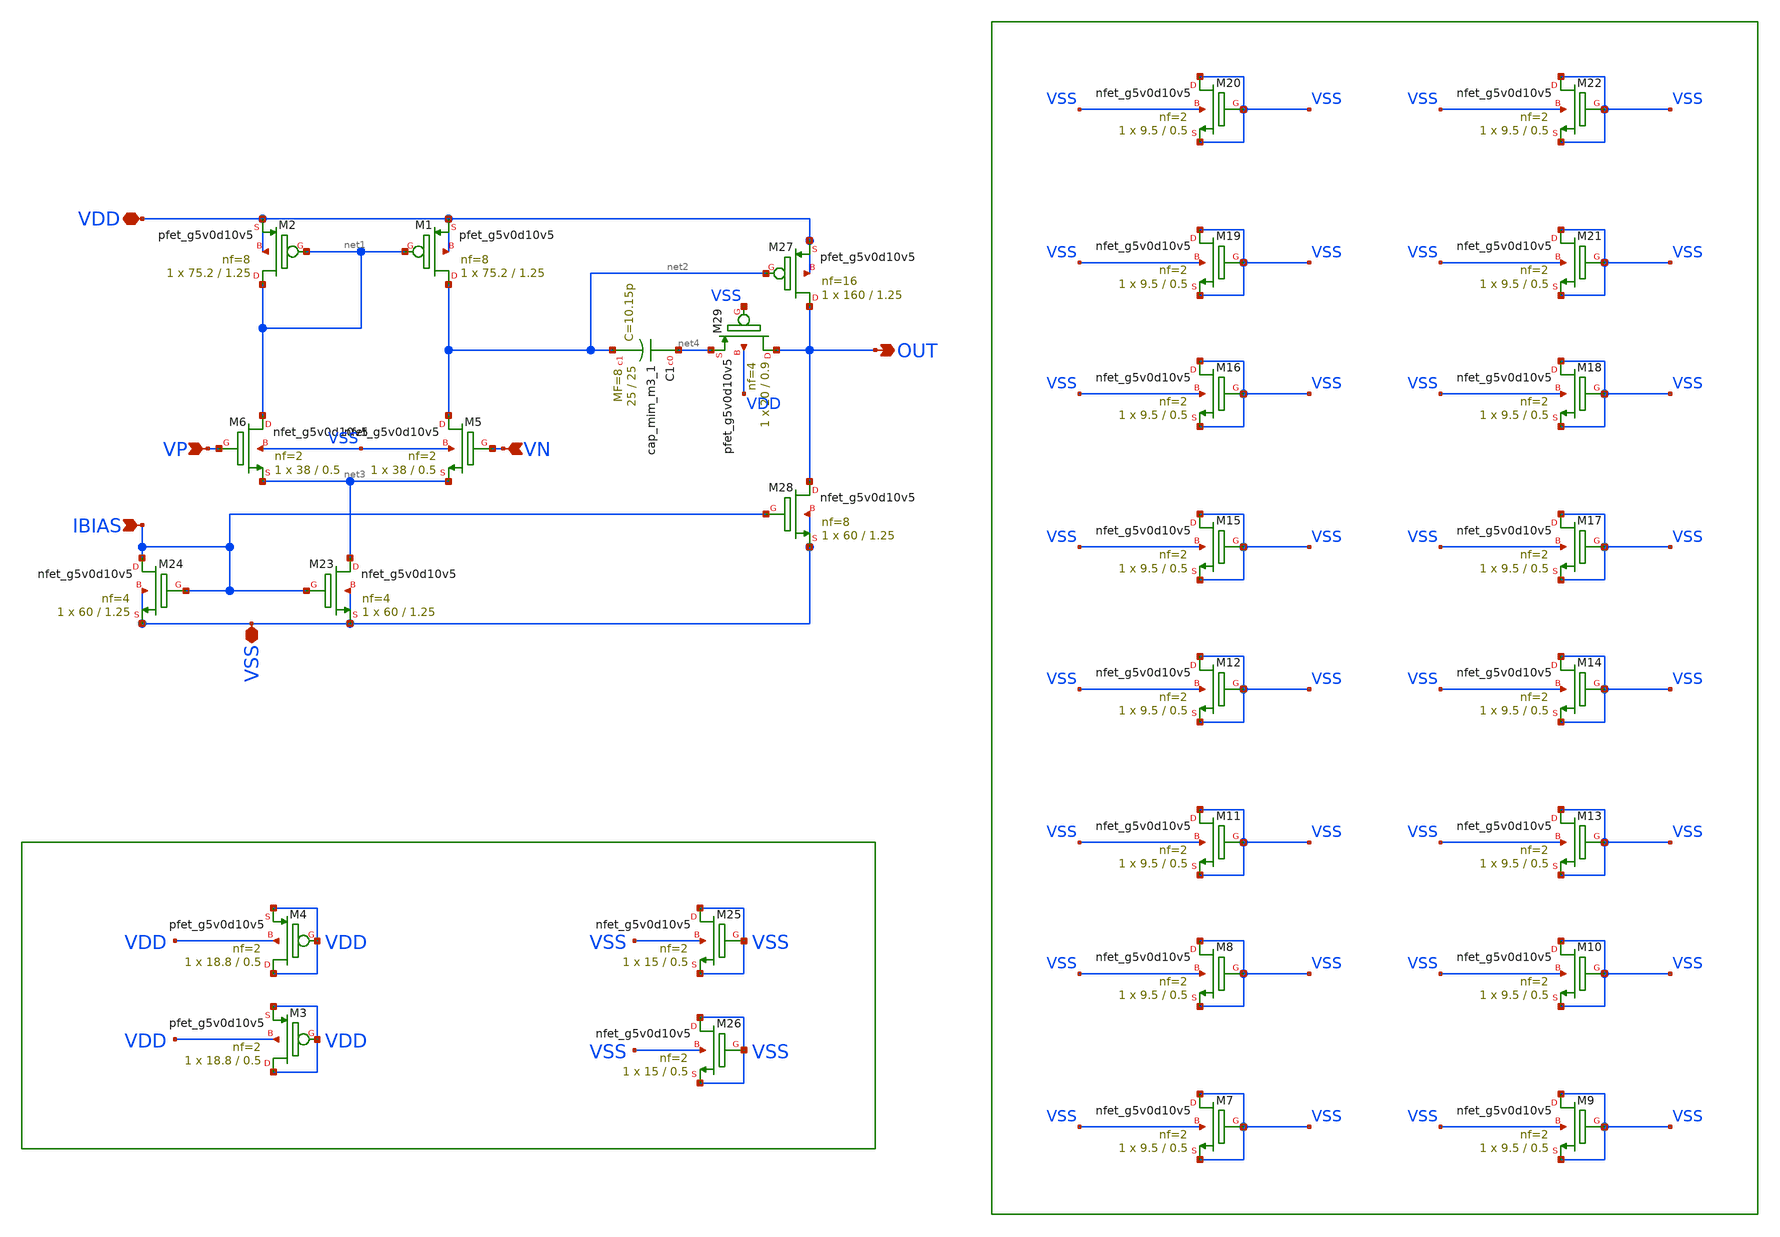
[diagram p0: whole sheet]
** sch_path: xschem/error-amplifier2/schematics/1st-stage.sch
**.subckt 1st-stage VDD VP VN IBIAS VSS OUT
*.iopin VDD
*.ipin VP
*.ipin VN
*.ipin IBIAS
*.iopin VSS
*.opin OUT
XM1 net2 net1 VDD VDD sky130_fd_pr__pfet_g5v0d10v5 L=1.25 W=75.2 nf=8 ad='int((nf+1)/2) * W/nf * 0.29'
+ as='int((nf+2)/2) * W/nf * 0.29' pd='2*int((nf+1)/2) * (W/nf + 0.29)' ps='2*int((nf+2)/2) * (W/nf + 0.29)'
+ nrd='0.29 / W' nrs='0.29 / W' sa=0 sb=0 sd=0 mult=1 m=1
XM2 net1 net1 VDD VDD sky130_fd_pr__pfet_g5v0d10v5 L=1.25 W=75.2 nf=8 ad='int((nf+1)/2) * W/nf * 0.29'
+ as='int((nf+2)/2) * W/nf * 0.29' pd='2*int((nf+1)/2) * (W/nf + 0.29)' ps='2*int((nf+2)/2) * (W/nf + 0.29)'
+ nrd='0.29 / W' nrs='0.29 / W' sa=0 sb=0 sd=0 mult=1 m=1
XM3 VDD VDD VDD VDD sky130_fd_pr__pfet_g5v0d10v5 L=0.5 W=18.8 nf=2 ad='int((nf+1)/2) * W/nf * 0.29' as='int((nf+2)/2) * W/nf * 0.29'
+ pd='2*int((nf+1)/2) * (W/nf + 0.29)' ps='2*int((nf+2)/2) * (W/nf + 0.29)' nrd='0.29 / W' nrs='0.29 / W'
+ sa=0 sb=0 sd=0 mult=1 m=1
XM4 VDD VDD VDD VDD sky130_fd_pr__pfet_g5v0d10v5 L=0.5 W=18.8 nf=2 ad='int((nf+1)/2) * W/nf * 0.29' as='int((nf+2)/2) * W/nf * 0.29'
+ pd='2*int((nf+1)/2) * (W/nf + 0.29)' ps='2*int((nf+2)/2) * (W/nf + 0.29)' nrd='0.29 / W' nrs='0.29 / W'
+ sa=0 sb=0 sd=0 mult=1 m=1
XM5 net2 VN net3 VSS sky130_fd_pr__nfet_g5v0d10v5 L=0.5 W=38 nf=2 ad='int((nf+1)/2) * W/nf * 0.29' as='int((nf+2)/2) * W/nf * 0.29'
+ pd='2*int((nf+1)/2) * (W/nf + 0.29)' ps='2*int((nf+2)/2) * (W/nf + 0.29)' nrd='0.29 / W' nrs='0.29 / W'
+ sa=0 sb=0 sd=0 mult=1 m=1
XM6 net1 VP net3 VSS sky130_fd_pr__nfet_g5v0d10v5 L=0.5 W=38 nf=2 ad='int((nf+1)/2) * W/nf * 0.29' as='int((nf+2)/2) * W/nf * 0.29'
+ pd='2*int((nf+1)/2) * (W/nf + 0.29)' ps='2*int((nf+2)/2) * (W/nf + 0.29)' nrd='0.29 / W' nrs='0.29 / W'
+ sa=0 sb=0 sd=0 mult=1 m=1
XM7 VSS VSS VSS VSS sky130_fd_pr__nfet_g5v0d10v5 L=0.5 W=9.5 nf=2 ad='int((nf+1)/2) * W/nf * 0.29' as='int((nf+2)/2) * W/nf * 0.29'
+ pd='2*int((nf+1)/2) * (W/nf + 0.29)' ps='2*int((nf+2)/2) * (W/nf + 0.29)' nrd='0.29 / W' nrs='0.29 / W'
+ sa=0 sb=0 sd=0 mult=1 m=1
XM8 VSS VSS VSS VSS sky130_fd_pr__nfet_g5v0d10v5 L=0.5 W=9.5 nf=2 ad='int((nf+1)/2) * W/nf * 0.29' as='int((nf+2)/2) * W/nf * 0.29'
+ pd='2*int((nf+1)/2) * (W/nf + 0.29)' ps='2*int((nf+2)/2) * (W/nf + 0.29)' nrd='0.29 / W' nrs='0.29 / W'
+ sa=0 sb=0 sd=0 mult=1 m=1
XM9 VSS VSS VSS VSS sky130_fd_pr__nfet_g5v0d10v5 L=0.5 W=9.5 nf=2 ad='int((nf+1)/2) * W/nf * 0.29' as='int((nf+2)/2) * W/nf * 0.29'
+ pd='2*int((nf+1)/2) * (W/nf + 0.29)' ps='2*int((nf+2)/2) * (W/nf + 0.29)' nrd='0.29 / W' nrs='0.29 / W'
+ sa=0 sb=0 sd=0 mult=1 m=1
XM10 VSS VSS VSS VSS sky130_fd_pr__nfet_g5v0d10v5 L=0.5 W=9.5 nf=2 ad='int((nf+1)/2) * W/nf * 0.29' as='int((nf+2)/2) * W/nf * 0.29'
+ pd='2*int((nf+1)/2) * (W/nf + 0.29)' ps='2*int((nf+2)/2) * (W/nf + 0.29)' nrd='0.29 / W' nrs='0.29 / W'
+ sa=0 sb=0 sd=0 mult=1 m=1
XM11 VSS VSS VSS VSS sky130_fd_pr__nfet_g5v0d10v5 L=0.5 W=9.5 nf=2 ad='int((nf+1)/2) * W/nf * 0.29' as='int((nf+2)/2) * W/nf * 0.29'
+ pd='2*int((nf+1)/2) * (W/nf + 0.29)' ps='2*int((nf+2)/2) * (W/nf + 0.29)' nrd='0.29 / W' nrs='0.29 / W'
+ sa=0 sb=0 sd=0 mult=1 m=1
XM12 VSS VSS VSS VSS sky130_fd_pr__nfet_g5v0d10v5 L=0.5 W=9.5 nf=2 ad='int((nf+1)/2) * W/nf * 0.29' as='int((nf+2)/2) * W/nf * 0.29'
+ pd='2*int((nf+1)/2) * (W/nf + 0.29)' ps='2*int((nf+2)/2) * (W/nf + 0.29)' nrd='0.29 / W' nrs='0.29 / W'
+ sa=0 sb=0 sd=0 mult=1 m=1
XM13 VSS VSS VSS VSS sky130_fd_pr__nfet_g5v0d10v5 L=0.5 W=9.5 nf=2 ad='int((nf+1)/2) * W/nf * 0.29' as='int((nf+2)/2) * W/nf * 0.29'
+ pd='2*int((nf+1)/2) * (W/nf + 0.29)' ps='2*int((nf+2)/2) * (W/nf + 0.29)' nrd='0.29 / W' nrs='0.29 / W'
+ sa=0 sb=0 sd=0 mult=1 m=1
XM14 VSS VSS VSS VSS sky130_fd_pr__nfet_g5v0d10v5 L=0.5 W=9.5 nf=2 ad='int((nf+1)/2) * W/nf * 0.29' as='int((nf+2)/2) * W/nf * 0.29'
+ pd='2*int((nf+1)/2) * (W/nf + 0.29)' ps='2*int((nf+2)/2) * (W/nf + 0.29)' nrd='0.29 / W' nrs='0.29 / W'
+ sa=0 sb=0 sd=0 mult=1 m=1
XM15 VSS VSS VSS VSS sky130_fd_pr__nfet_g5v0d10v5 L=0.5 W=9.5 nf=2 ad='int((nf+1)/2) * W/nf * 0.29' as='int((nf+2)/2) * W/nf * 0.29'
+ pd='2*int((nf+1)/2) * (W/nf + 0.29)' ps='2*int((nf+2)/2) * (W/nf + 0.29)' nrd='0.29 / W' nrs='0.29 / W'
+ sa=0 sb=0 sd=0 mult=1 m=1
XM16 VSS VSS VSS VSS sky130_fd_pr__nfet_g5v0d10v5 L=0.5 W=9.5 nf=2 ad='int((nf+1)/2) * W/nf * 0.29' as='int((nf+2)/2) * W/nf * 0.29'
+ pd='2*int((nf+1)/2) * (W/nf + 0.29)' ps='2*int((nf+2)/2) * (W/nf + 0.29)' nrd='0.29 / W' nrs='0.29 / W'
+ sa=0 sb=0 sd=0 mult=1 m=1
XM17 VSS VSS VSS VSS sky130_fd_pr__nfet_g5v0d10v5 L=0.5 W=9.5 nf=2 ad='int((nf+1)/2) * W/nf * 0.29' as='int((nf+2)/2) * W/nf * 0.29'
+ pd='2*int((nf+1)/2) * (W/nf + 0.29)' ps='2*int((nf+2)/2) * (W/nf + 0.29)' nrd='0.29 / W' nrs='0.29 / W'
+ sa=0 sb=0 sd=0 mult=1 m=1
XM18 VSS VSS VSS VSS sky130_fd_pr__nfet_g5v0d10v5 L=0.5 W=9.5 nf=2 ad='int((nf+1)/2) * W/nf * 0.29' as='int((nf+2)/2) * W/nf * 0.29'
+ pd='2*int((nf+1)/2) * (W/nf + 0.29)' ps='2*int((nf+2)/2) * (W/nf + 0.29)' nrd='0.29 / W' nrs='0.29 / W'
+ sa=0 sb=0 sd=0 mult=1 m=1
XM19 VSS VSS VSS VSS sky130_fd_pr__nfet_g5v0d10v5 L=0.5 W=9.5 nf=2 ad='int((nf+1)/2) * W/nf * 0.29' as='int((nf+2)/2) * W/nf * 0.29'
+ pd='2*int((nf+1)/2) * (W/nf + 0.29)' ps='2*int((nf+2)/2) * (W/nf + 0.29)' nrd='0.29 / W' nrs='0.29 / W'
+ sa=0 sb=0 sd=0 mult=1 m=1
XM20 VSS VSS VSS VSS sky130_fd_pr__nfet_g5v0d10v5 L=0.5 W=9.5 nf=2 ad='int((nf+1)/2) * W/nf * 0.29' as='int((nf+2)/2) * W/nf * 0.29'
+ pd='2*int((nf+1)/2) * (W/nf + 0.29)' ps='2*int((nf+2)/2) * (W/nf + 0.29)' nrd='0.29 / W' nrs='0.29 / W'
+ sa=0 sb=0 sd=0 mult=1 m=1
XM21 VSS VSS VSS VSS sky130_fd_pr__nfet_g5v0d10v5 L=0.5 W=9.5 nf=2 ad='int((nf+1)/2) * W/nf * 0.29' as='int((nf+2)/2) * W/nf * 0.29'
+ pd='2*int((nf+1)/2) * (W/nf + 0.29)' ps='2*int((nf+2)/2) * (W/nf + 0.29)' nrd='0.29 / W' nrs='0.29 / W'
+ sa=0 sb=0 sd=0 mult=1 m=1
XM22 VSS VSS VSS VSS sky130_fd_pr__nfet_g5v0d10v5 L=0.5 W=9.5 nf=2 ad='int((nf+1)/2) * W/nf * 0.29' as='int((nf+2)/2) * W/nf * 0.29'
+ pd='2*int((nf+1)/2) * (W/nf + 0.29)' ps='2*int((nf+2)/2) * (W/nf + 0.29)' nrd='0.29 / W' nrs='0.29 / W'
+ sa=0 sb=0 sd=0 mult=1 m=1
XM23 net3 IBIAS VSS VSS sky130_fd_pr__nfet_g5v0d10v5 L=1.25 W=60 nf=4 ad='int((nf+1)/2) * W/nf * 0.29'
+ as='int((nf+2)/2) * W/nf * 0.29' pd='2*int((nf+1)/2) * (W/nf + 0.29)' ps='2*int((nf+2)/2) * (W/nf + 0.29)'
+ nrd='0.29 / W' nrs='0.29 / W' sa=0 sb=0 sd=0 mult=1 m=1
XM24 IBIAS IBIAS VSS VSS sky130_fd_pr__nfet_g5v0d10v5 L=1.25 W=60 nf=4 ad='int((nf+1)/2) * W/nf * 0.29'
+ as='int((nf+2)/2) * W/nf * 0.29' pd='2*int((nf+1)/2) * (W/nf + 0.29)' ps='2*int((nf+2)/2) * (W/nf + 0.29)'
+ nrd='0.29 / W' nrs='0.29 / W' sa=0 sb=0 sd=0 mult=1 m=1
XM25 VSS VSS VSS VSS sky130_fd_pr__nfet_g5v0d10v5 L=0.5 W=15 nf=2 ad='int((nf+1)/2) * W/nf * 0.29' as='int((nf+2)/2) * W/nf * 0.29'
+ pd='2*int((nf+1)/2) * (W/nf + 0.29)' ps='2*int((nf+2)/2) * (W/nf + 0.29)' nrd='0.29 / W' nrs='0.29 / W'
+ sa=0 sb=0 sd=0 mult=1 m=1
XM26 VSS VSS VSS VSS sky130_fd_pr__nfet_g5v0d10v5 L=0.5 W=15 nf=2 ad='int((nf+1)/2) * W/nf * 0.29' as='int((nf+2)/2) * W/nf * 0.29'
+ pd='2*int((nf+1)/2) * (W/nf + 0.29)' ps='2*int((nf+2)/2) * (W/nf + 0.29)' nrd='0.29 / W' nrs='0.29 / W'
+ sa=0 sb=0 sd=0 mult=1 m=1
XM27 OUT net2 VDD VDD sky130_fd_pr__pfet_g5v0d10v5 L=1.25 W=160 nf=16 ad='int((nf+1)/2) * W/nf * 0.29'
+ as='int((nf+2)/2) * W/nf * 0.29' pd='2*int((nf+1)/2) * (W/nf + 0.29)' ps='2*int((nf+2)/2) * (W/nf + 0.29)'
+ nrd='0.29 / W' nrs='0.29 / W' sa=0 sb=0 sd=0 mult=1 m=1
XM28 OUT IBIAS VSS VSS sky130_fd_pr__nfet_g5v0d10v5 L=1.25 W=60 nf=8 ad='int((nf+1)/2) * W/nf * 0.29'
+ as='int((nf+2)/2) * W/nf * 0.29' pd='2*int((nf+1)/2) * (W/nf + 0.29)' ps='2*int((nf+2)/2) * (W/nf + 0.29)'
+ nrd='0.29 / W' nrs='0.29 / W' sa=0 sb=0 sd=0 mult=1 m=1
XC1 net4 net2 sky130_fd_pr__cap_mim_m3_1 W=25 L=25 MF=8 m=8
XM29 OUT VSS net4 VDD sky130_fd_pr__pfet_g5v0d10v5 L=0.9 W=20 nf=4 ad='int((nf+1)/2) * W/nf * 0.29' as='int((nf+2)/2) * W/nf * 0.29'
+ pd='2*int((nf+1)/2) * (W/nf + 0.29)' ps='2*int((nf+2)/2) * (W/nf + 0.29)' nrd='0.29 / W' nrs='0.29 / W'
+ sa=0 sb=0 sd=0 mult=1 m=1
**.ends
.end
